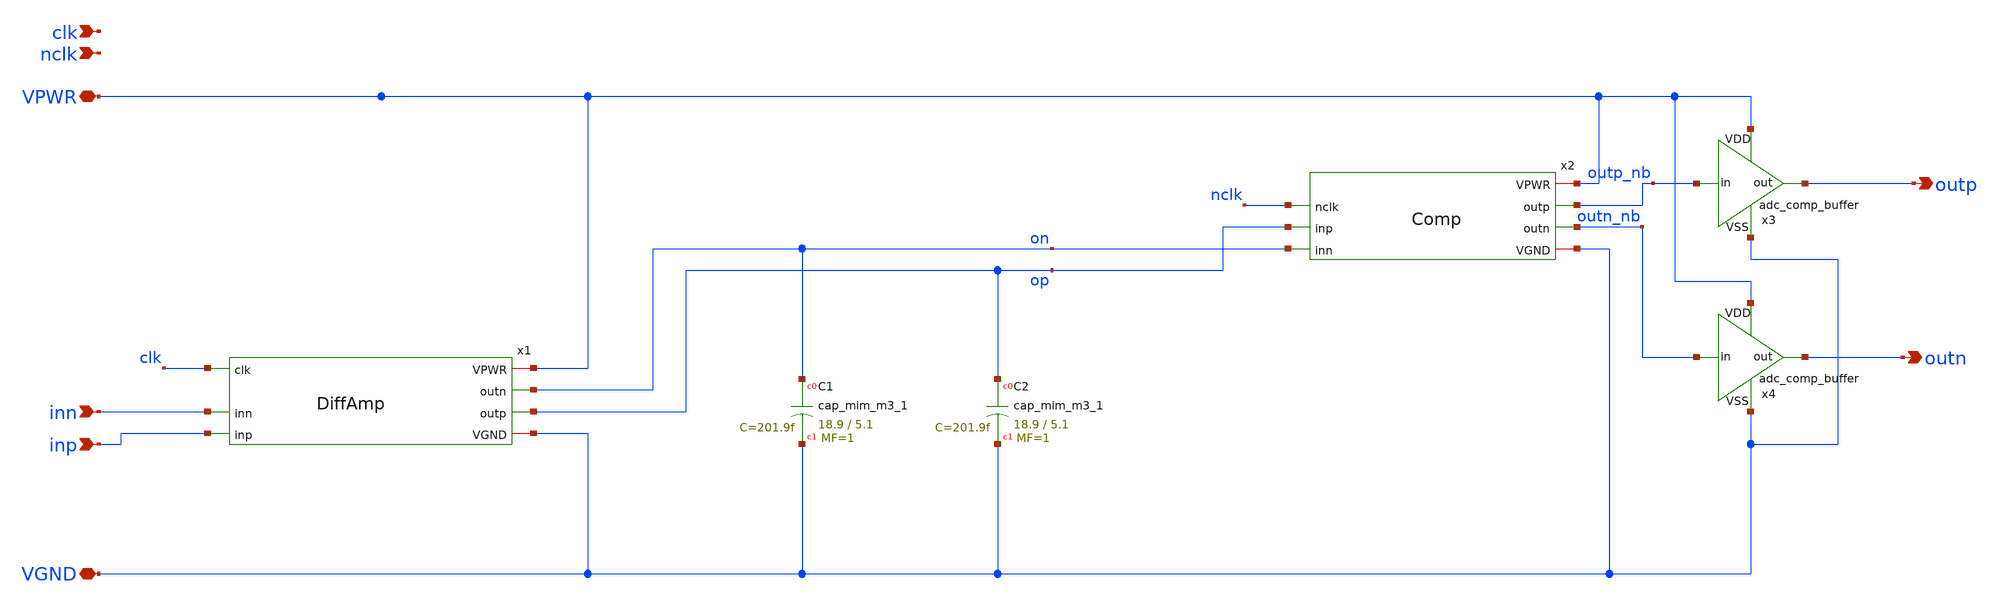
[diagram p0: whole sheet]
** sch_path: Circuits/Comparator/adc_comp.sch
* Circuits/Comparator/adc_comp_buffer.sch:
* Copyright 2022 Manuel Moser
* Licensed under the Apache License, Version 2.0 (the "License");
**.subckt adc_comp VPWR VGND clk nclk inp inn outp outn
*.iopin VPWR
*.iopin VGND
*.ipin clk
*.ipin nclk
*.ipin inp
*.ipin inn
*.opin outp
*.opin outn
XC1 on VGND sky130_fd_pr__cap_mim_m3_1 W=18.9 L=5.1 MF=1 m=1
XC2 op VGND sky130_fd_pr__cap_mim_m3_1 W=18.9 L=5.1 MF=1 m=1
x1 clk VPWR on op inn inp VGND DiffAmp
x2 nclk VPWR outp_nb op on outn_nb VGND Comp
x3 VPWR VGND outp_nb outp adc_comp_buffer
x4 VPWR VGND outn_nb outn adc_comp_buffer
**.ends

* expanding   symbol:
*+  /home/jakob/Documents/AutomatedLayoutGeneration/Circuits/Comparator/DiffAmp.sym # of pins=7
** sym_path: Circuits/Comparator/DiffAmp.sym
** sch_path: Circuits/Comparator/DiffAmp.sch
.subckt DiffAmp clk VPWR outn outp inn inp VGND
*.iopin VPWR
*.iopin VGND
*.ipin clk
*.ipin inp
*.ipin inn
*.opin outn
*.opin outp
XM3 outn inp in_stage_net1 VGND sky130_fd_pr__nfet_01v8 L=0.3 W=8 nf=4 ad='int((nf+1)/2) * W/nf * 0.29'
+ as='int((nf+2)/2) * W/nf * 0.29' pd='2*int((nf+1)/2) * (W/nf + 0.29)' ps='2*int((nf+2)/2) * (W/nf + 0.29)'
+ nrd='0.29 / W' nrs='0.29 / W' sa=0 sb=0 sd=0 mult=1 m=1
XM4 outp inn in_stage_net1 VGND sky130_fd_pr__nfet_01v8 L=0.3 W=8 nf=4 ad='int((nf+1)/2) * W/nf * 0.29'
+ as='int((nf+2)/2) * W/nf * 0.29' pd='2*int((nf+1)/2) * (W/nf + 0.29)' ps='2*int((nf+2)/2) * (W/nf + 0.29)'
+ nrd='0.29 / W' nrs='0.29 / W' sa=0 sb=0 sd=0 mult=1 m=1
XM5 in_stage_net1 clk VGND VGND sky130_fd_pr__nfet_01v8 L=0.3 W=4 nf=8 ad='int((nf+1)/2) * W/nf * 0.29'
+ as='int((nf+2)/2) * W/nf * 0.29' pd='2*int((nf+1)/2) * (W/nf + 0.29)' ps='2*int((nf+2)/2) * (W/nf + 0.29)'
+ nrd='0.29 / W' nrs='0.29 / W' sa=0 sb=0 sd=0 mult=1 m=1
XM2 outp clk VPWR VPWR sky130_fd_pr__pfet_01v8 L=0.3 W=2 nf=4 ad='int((nf+1)/2) * W/nf * 0.29' as='int((nf+2)/2) * W/nf * 0.29'
+ pd='2*int((nf+1)/2) * (W/nf + 0.29)' ps='2*int((nf+2)/2) * (W/nf + 0.29)' nrd='0.29 / W' nrs='0.29 / W'
+ sa=0 sb=0 sd=0 mult=1 m=1
XM1 outn clk VPWR VPWR sky130_fd_pr__pfet_01v8 L=0.3 W=2 nf=4 ad='int((nf+1)/2) * W/nf * 0.29' as='int((nf+2)/2) * W/nf * 0.29'
+ pd='2*int((nf+1)/2) * (W/nf + 0.29)' ps='2*int((nf+2)/2) * (W/nf + 0.29)' nrd='0.29 / W' nrs='0.29 / W'
+ sa=0 sb=0 sd=0 mult=1 m=1
.ends


* expanding   symbol:  /home/jakob/Documents/AutomatedLayoutGeneration/Circuits/Comparator/Comp.sym
*+ # of pins=7
** sym_path: Circuits/Comparator/Comp.sym
** sch_path: Circuits/Comparator/Comp.sch
.subckt Comp nclk VPWR outp inp inn outn VGND
*.opin outp
*.opin outn
*.iopin VPWR
*.ipin nclk
*.iopin VGND
*.ipin inp
*.ipin inn
XM6 in_stage_net2 outp VPWR VPWR sky130_fd_pr__pfet_01v8 L=0.3 W=4 nf=2 ad='int((nf+1)/2) * W/nf * 0.29'
+ as='int((nf+2)/2) * W/nf * 0.29' pd='2*int((nf+1)/2) * (W/nf + 0.29)' ps='2*int((nf+2)/2) * (W/nf + 0.29)'
+ nrd='0.29 / W' nrs='0.29 / W' sa=0 sb=0 sd=0 mult=1 m=1
XM7 in_stage_net3 outn VPWR VPWR sky130_fd_pr__pfet_01v8 L=0.3 W=4 nf=2 ad='int((nf+1)/2) * W/nf * 0.29'
+ as='int((nf+2)/2) * W/nf * 0.29' pd='2*int((nf+1)/2) * (W/nf + 0.29)' ps='2*int((nf+2)/2) * (W/nf + 0.29)'
+ nrd='0.29 / W' nrs='0.29 / W' sa=0 sb=0 sd=0 mult=1 m=1
XM8 outn inn in_stage_net2 VPWR sky130_fd_pr__pfet_01v8 L=0.3 W=4 nf=2 ad='int((nf+1)/2) * W/nf * 0.29'
+ as='int((nf+2)/2) * W/nf * 0.29' pd='2*int((nf+1)/2) * (W/nf + 0.29)' ps='2*int((nf+2)/2) * (W/nf + 0.29)'
+ nrd='0.29 / W' nrs='0.29 / W' sa=0 sb=0 sd=0 mult=1 m=1
XM9 outp inp in_stage_net3 VPWR sky130_fd_pr__pfet_01v8 L=0.3 W=4 nf=2 ad='int((nf+1)/2) * W/nf * 0.29'
+ as='int((nf+2)/2) * W/nf * 0.29' pd='2*int((nf+1)/2) * (W/nf + 0.29)' ps='2*int((nf+2)/2) * (W/nf + 0.29)'
+ nrd='0.29 / W' nrs='0.29 / W' sa=0 sb=0 sd=0 mult=1 m=1
XM10 outn outp VGND VGND sky130_fd_pr__nfet_01v8 L=0.3 W=2 nf=1 ad='int((nf+1)/2) * W/nf * 0.29' as='int((nf+2)/2) * W/nf * 0.29'
+ pd='2*int((nf+1)/2) * (W/nf + 0.29)' ps='2*int((nf+2)/2) * (W/nf + 0.29)' nrd='0.29 / W' nrs='0.29 / W'
+ sa=0 sb=0 sd=0 mult=1 m=1
XM11 outn nclk VGND VGND sky130_fd_pr__nfet_01v8 L=0.3 W=2 nf=1 ad='int((nf+1)/2) * W/nf * 0.29' as='int((nf+2)/2) * W/nf * 0.29'
+ pd='2*int((nf+1)/2) * (W/nf + 0.29)' ps='2*int((nf+2)/2) * (W/nf + 0.29)' nrd='0.29 / W' nrs='0.29 / W'
+ sa=0 sb=0 sd=0 mult=1 m=1
XM12 outp nclk VGND VGND sky130_fd_pr__nfet_01v8 L=0.3 W=2 nf=1 ad='int((nf+1)/2) * W/nf * 0.29' as='int((nf+2)/2) * W/nf * 0.29'
+ pd='2*int((nf+1)/2) * (W/nf + 0.29)' ps='2*int((nf+2)/2) * (W/nf + 0.29)' nrd='0.29 / W' nrs='0.29 / W'
+ sa=0 sb=0 sd=0 mult=1 m=1
XM13 outp outn VGND VGND sky130_fd_pr__nfet_01v8 L=0.3 W=2 nf=1 ad='int((nf+1)/2) * W/nf * 0.29' as='int((nf+2)/2) * W/nf * 0.29'
+ pd='2*int((nf+1)/2) * (W/nf + 0.29)' ps='2*int((nf+2)/2) * (W/nf + 0.29)' nrd='0.29 / W' nrs='0.29 / W'
+ sa=0 sb=0 sd=0 mult=1 m=1
.ends


* expanding   symbol:  adc_comp_buffer.sym # of pins=4
** sym_path: adc_comp_buffer.sym
** sch_path: adc_comp_buffer.sch
.subckt adc_comp_buffer VDD VSS in out
*.iopin VDD
*.iopin VSS
*.ipin in
*.opin out
XM5 buf_mid in VSS VSS sky130_fd_pr__nfet_01v8 L=0.3 W=0.5 nf=1 ad='int((nf+1)/2) * W/nf * 0.29' as='int((nf+2)/2) * W/nf * 0.29'
+ pd='2*int((nf+1)/2) * (W/nf + 0.29)' ps='2*int((nf+2)/2) * (W/nf + 0.29)' nrd='0.29 / W' nrs='0.29 / W'
+ sa=0 sb=0 sd=0 mult=1 m=1
XM1 buf_mid in VDD VDD sky130_fd_pr__pfet_01v8 L=0.3 W=1 nf=1 ad='int((nf+1)/2) * W/nf * 0.29' as='int((nf+2)/2) * W/nf * 0.29'
+ pd='2*int((nf+1)/2) * (W/nf + 0.29)' ps='2*int((nf+2)/2) * (W/nf + 0.29)' nrd='0.29 / W' nrs='0.29 / W'
+ sa=0 sb=0 sd=0 mult=1 m=1
XM2 out buf_mid VDD VDD sky130_fd_pr__pfet_01v8 L=0.3 W=2 nf=2 ad='int((nf+1)/2) * W/nf * 0.29' as='int((nf+2)/2) * W/nf * 0.29'
+ pd='2*int((nf+1)/2) * (W/nf + 0.29)' ps='2*int((nf+2)/2) * (W/nf + 0.29)' nrd='0.29 / W' nrs='0.29 / W'
+ sa=0 sb=0 sd=0 mult=1 m=1
XM6 out buf_mid VSS VSS sky130_fd_pr__nfet_01v8 L=0.3 W=1 nf=2 ad='int((nf+1)/2) * W/nf * 0.29' as='int((nf+2)/2) * W/nf * 0.29'
+ pd='2*int((nf+1)/2) * (W/nf + 0.29)' ps='2*int((nf+2)/2) * (W/nf + 0.29)' nrd='0.29 / W' nrs='0.29 / W'
+ sa=0 sb=0 sd=0 mult=1 m=1
.ends

.end
